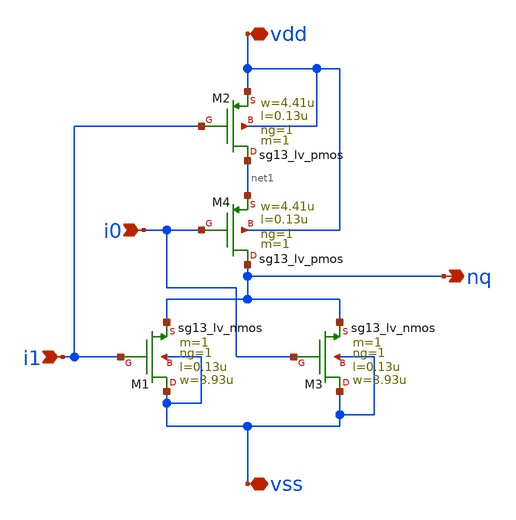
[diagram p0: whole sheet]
** sch_path: ihp-sg13g2/libs.ref/sg13g2_io/xschem/sg13g2_io_nor2_x1.sch
**.subckt sg13g2_io_nor2_x1 vss vdd i0 i1 nq
*.iopin vss
*.iopin vdd
*.ipin i0
*.ipin i1
*.opin nq
XM1 vss i1 nq vss sg13_lv_nmos w=3.93u l=0.13u ng=1 m=1 mm_ok=1
XM2 net1 i1 vdd vdd sg13_lv_pmos w=4.41u l=0.13u ng=1 m=1 mm_ok=1
XM3 vss i0 nq vss sg13_lv_nmos w=3.93u l=0.13u ng=1 m=1 mm_ok=1
XM4 nq i0 net1 vdd sg13_lv_pmos w=4.41u l=0.13u ng=1 m=1 mm_ok=1
**.ends
.end
